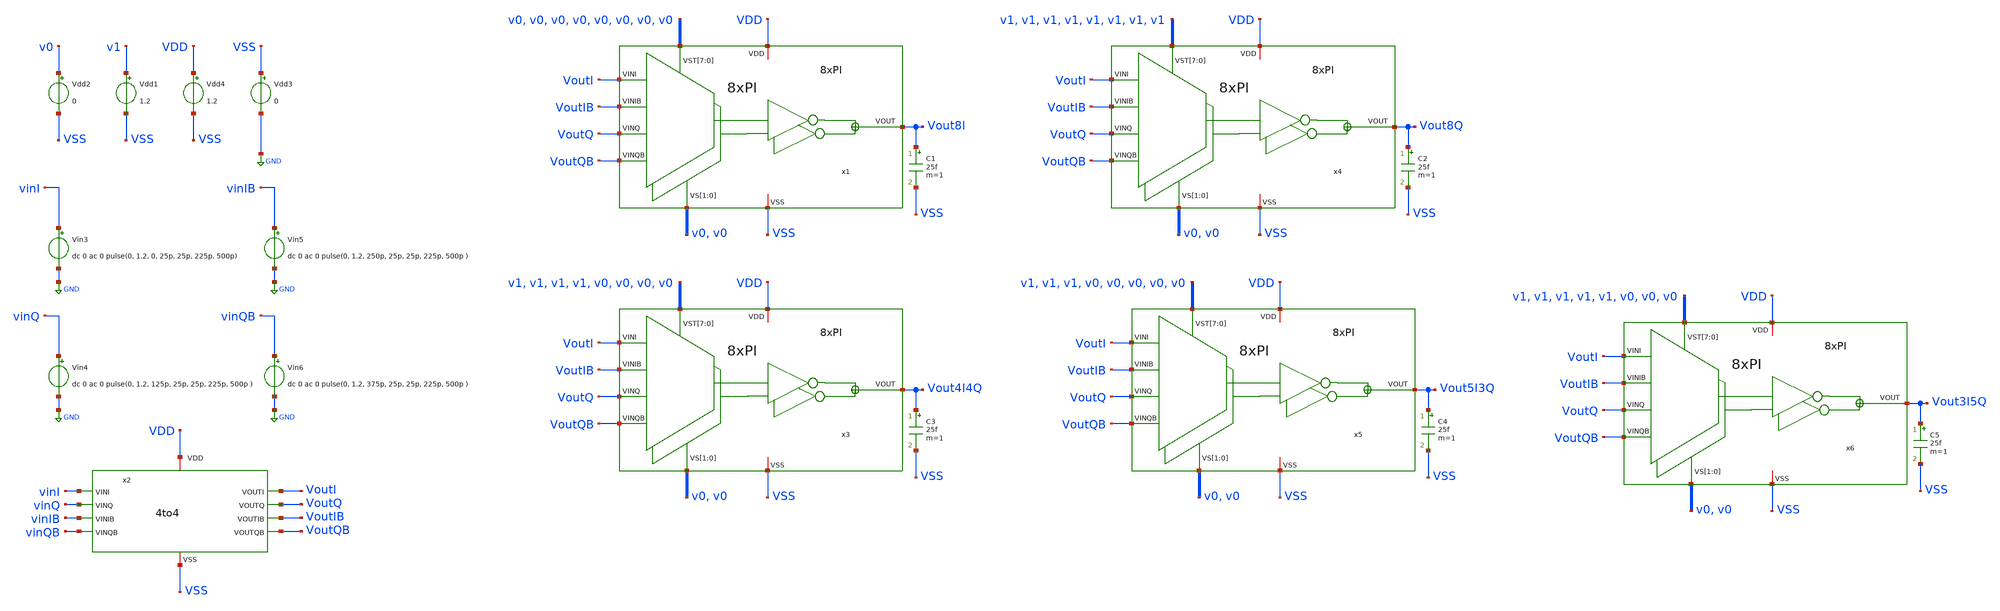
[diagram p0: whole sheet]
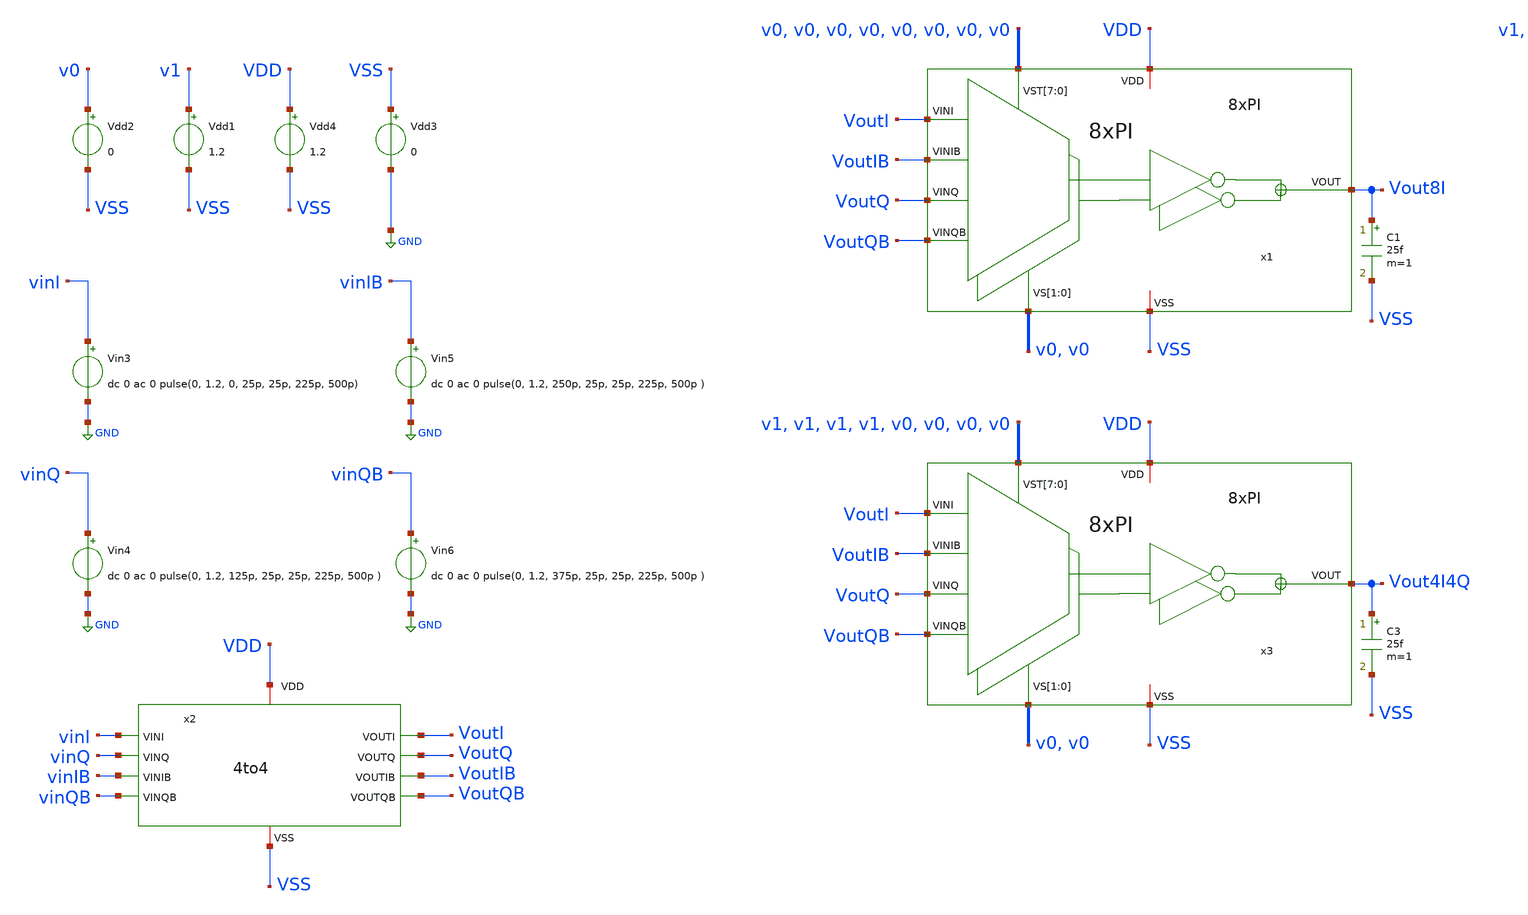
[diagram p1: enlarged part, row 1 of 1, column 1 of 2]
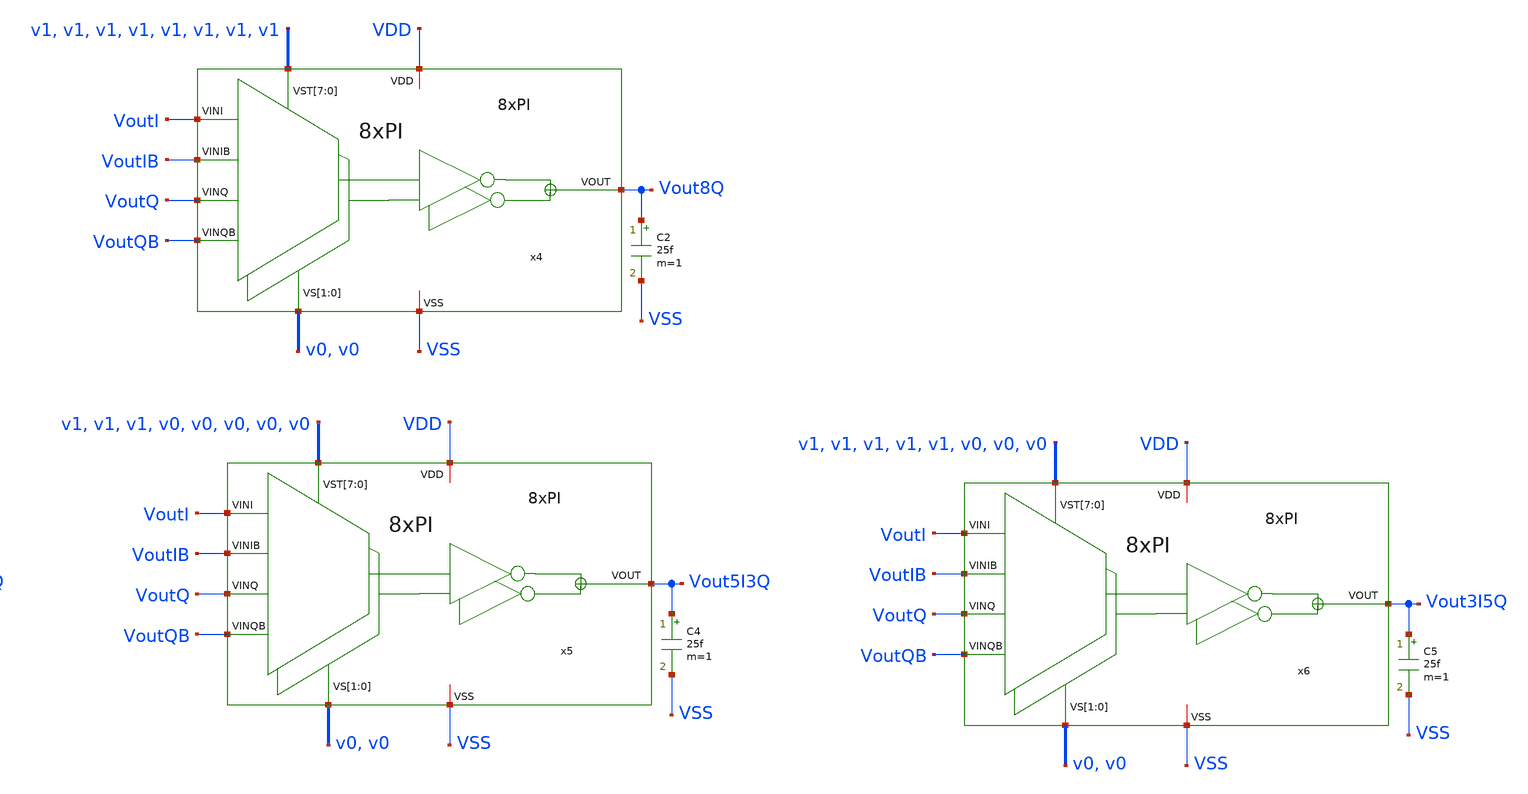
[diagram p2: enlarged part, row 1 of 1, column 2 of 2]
** sch_path: 8xPI/tb_8xPI.sch
**.subckt tb_8xPI
x1 VoutI VoutIB VoutQ VoutQB v0 v0 v0 v0 v0 v0 v0 v0 v0 v0 Vout8I VDD VSS 8xPI
Vin3 vinI GND dc 0 ac 0 pulse(0, 1.2, 0, 25p, 25p, 225p, 500p)
Vin4 vinQ GND dc 0 ac 0 pulse(0, 1.2, 125p, 25p, 25p, 225p, 500p )
Vin5 vinIB GND dc 0 ac 0 pulse(0, 1.2, 250p, 25p, 25p, 225p, 500p )
Vin6 vinQB GND dc 0 ac 0 pulse(0, 1.2, 375p, 25p, 25p, 225p, 500p )
x2 VDD vinI VoutI VoutQ vinQ vinIB VoutIB vinQB VoutQB VSS 4to4
Vdd4 VDD VSS 1.2
Vdd1 v1 VSS 1.2
Vdd2 v0 VSS 0
Vdd3 VSS GND 0
x3 VoutI VoutIB VoutQ VoutQB v0 v0 v1 v1 v1 v1 v0 v0 v0 v0 Vout4I4Q VDD VSS 8xPI
x4 VoutI VoutIB VoutQ VoutQB v0 v0 v1 v1 v1 v1 v1 v1 v1 v1 Vout8Q VDD VSS 8xPI
x5 VoutI VoutIB VoutQ VoutQB v0 v0 v1 v1 v1 v0 v0 v0 v0 v0 Vout5I3Q VDD VSS 8xPI
x6 VoutI VoutIB VoutQ VoutQB v0 v0 v1 v1 v1 v1 v1 v0 v0 v0 Vout3I5Q VDD VSS 8xPI
C1 Vout8I VSS 25f m=1
C2 Vout8Q VSS 25f m=1
C3 Vout4I4Q VSS 25f m=1
C4 Vout5I3Q VSS 25f m=1
C5 Vout3I5Q VSS 25f m=1
**** begin user architecture code


.param temp=27
.control
save all
tran 5p 1.5n

*meas tran tPWI TRIG v(Vout_I) VAl=0.6 RISE=1 TARG v(Vout_I) VAl=0.6 FALL=1
*meas tran tPWIQ TRIG v(Vout_IQ) VAl=0.6 RISE=1 TARG v(Vout_IQ) VAl=0.6 FALL=1
*meas tran tPWQ TRIG v(Vout_Q) VAl=0.6 RISE=1 TARG v(Vout_Q) VAl=0.6 FALL=1
*meas tran tPWQIB TRIG v(Vout_QIB) VAl=0.6 RISE=1 TARG v(Vout_QIB) VAl=0.6 FALL=1
*meas tran tPWIB TRIG v(Vout_IB) VAl=0.6 RISE=1 TARG v(Vout_IB) VAl=0.6 FALL=1
*meas tran tPWIBQB TRIG v(Vout_IBQB) VAl=0.6 RISE=1 TARG v(Vout_IBQB) VAl=0.6 FALL=1
*meas tran tPWQB TRIG v(Vout_QB) VAl=0.6 RISE=1 TARG v(Vout_QB) VAl=0.6 FALL=1
*meas tran tPWQBI TRIG v(Vout_QBI) VAl=0.6 RISE=1 TARG v(Vout_QBI) VAl=0.6 FALL=1


*meas tran tskewI_IQ TRIG v(Vout_I) VAl=0.6 RISE=1 TARG v(Vout_IQ) VAl=0.6 RISE=1
*meas tran tskewIQ_Q TRIG v(Vout_IQ) VAl=0.6 RISE=1 TARG v(Vout_Q) VAl=0.6 RISE=1
*meas tran tskewQ_QIB TRIG v(Vout_Q) VAl=0.6 RISE=1 TARG v(Vout_QIB) VAl=0.6 RISE=1
*meas tran tskewQIB_IB TRIG v(Vout_QIB) VAl=0.6 RISE=1 TARG v(Vout_IB) VAl=0.6 RISE=1
*meas tran tskewIB_IBQB TRIG v(Vout_IB) VAl=0.6 RISE=1 TARG v(Vout_IBQB) VAl=0.6 RISE=1
*meas tran tskewIBQB_QB TRIG v(Vout_IBQB) VAl=0.6 RISE=1 TARG v(Vout_QB) VAl=0.6 RISE=1
*meas tran tskewQB_QBI TRIG v(Vout_QB) VAl=0.6 RISE=1 TARG v(Vout_QBI) VAl=0.6 RISE=1
*meas tran tskewQBI_I TRIG v(Vout_QBI) VAl=0.6 RISE=1 TARG v(Vout_I) VAl=0.6 RISE=2


write tran_8XPI.raw
.endc



.lib cornerMOSlv.lib mos_tt

**** end user architecture code
**.ends

* expanding   symbol:  /foss/designs/PhaseInterpolator/8xPI/8xPI.sym # of pins=9
** sym_path: /foss/designs/PhaseInterpolator/8xPI/8xPI.sym
** sch_path: /foss/designs/PhaseInterpolator/8xPI/8xPI.sch
.subckt 8xPI VINI VINIB VINQ VINQB VS[1] VS[0] VST[7] VST[6] VST[5] VST[4] VST[3] VST[2] VST[1]
+ VST[0] VOUT VDD VSS
*.ipin VINI
*.ipin VINQ
*.ipin VINIB
*.ipin VINQB
*.iopin VDD
*.iopin VSS
*.opin VOUT
*.ipin VS[1],VS[0]
*.ipin VST[7],VST[6],VST[5],VST[4],VST[3],VST[2],VST[1],VST[0]
x1[7] VINI VINIB VDD net1 VS[1] VS[0] VINQ VSS VINQB VST[7] MUX_4_1
x1[6] VINI VINIB VDD net1 VS[1] VS[0] VINQ VSS VINQB VST[6] MUX_4_1
x1[5] VINI VINIB VDD net1 VS[1] VS[0] VINQ VSS VINQB VST[5] MUX_4_1
x1[4] VINI VINIB VDD net1 VS[1] VS[0] VINQ VSS VINQB VST[4] MUX_4_1
x1[3] VINI VINIB VDD net1 VS[1] VS[0] VINQ VSS VINQB VST[3] MUX_4_1
x1[2] VINI VINIB VDD net1 VS[1] VS[0] VINQ VSS VINQB VST[2] MUX_4_1
x1[1] VINI VINIB VDD net1 VS[1] VS[0] VINQ VSS VINQB VST[1] MUX_4_1
x1[0] VINI VINIB VDD net1 VS[1] VS[0] VINQ VSS VINQB VST[0] MUX_4_1
x2 VDD net2 net1 VSS inv
x3[1] VDD net3[1] net2 VSS inv
x3[0] VDD net3[0] net2 VSS inv
x4[3] VDD net4[3] net3[1] VSS inv
x4[2] VDD net4[2] net3[0] VSS inv
x4[1] VDD net4[1] net3[1] VSS inv
x4[0] VDD net4[0] net3[0] VSS inv
x5[7] VDD VOUT net4[3] VSS inv
x5[6] VDD VOUT net4[2] VSS inv
x5[5] VDD VOUT net4[1] VSS inv
x5[4] VDD VOUT net4[0] VSS inv
x5[3] VDD VOUT net4[3] VSS inv
x5[2] VDD VOUT net4[2] VSS inv
x5[1] VDD VOUT net4[1] VSS inv
x5[0] VDD VOUT net4[0] VSS inv
.ends


* expanding   symbol:  4to4.sym # of pins=10
** sym_path: 4to4.sym
** sch_path: 4to4.sch
.subckt 4to4 VDD VINI VOUTI VOUTQ VINQ VINIB VOUTIB VINQB VOUTQB VSS
*.iopin VDD
*.iopin VSS
*.ipin VINI
*.ipin VINQ
*.ipin VINIB
*.ipin VINQB
*.opin VOUTI
*.opin VOUTQ
*.opin VOUTIB
*.opin VOUTQB
x0[7] VDD net4[7] VINI VSS inv
x0[6] VDD net4[6] VINI VSS inv
x0[5] VDD net4[5] VINI VSS inv
x0[4] VDD net4[4] VINI VSS inv
x0[3] VDD net4[3] VINI VSS inv
x0[2] VDD net4[2] VINI VSS inv
x0[1] VDD net4[1] VINI VSS inv
x0[0] VDD net4[0] VINI VSS inv
x1[7] VDD net3[7] VINQ VSS inv
x1[6] VDD net3[6] VINQ VSS inv
x1[5] VDD net3[5] VINQ VSS inv
x1[4] VDD net3[4] VINQ VSS inv
x1[3] VDD net3[3] VINQ VSS inv
x1[2] VDD net3[2] VINQ VSS inv
x1[1] VDD net3[1] VINQ VSS inv
x1[0] VDD net3[0] VINQ VSS inv
x2[7] VDD net1[7] VINIB VSS inv
x2[6] VDD net1[6] VINIB VSS inv
x2[5] VDD net1[5] VINIB VSS inv
x2[4] VDD net1[4] VINIB VSS inv
x2[3] VDD net1[3] VINIB VSS inv
x2[2] VDD net1[2] VINIB VSS inv
x2[1] VDD net1[1] VINIB VSS inv
x2[0] VDD net1[0] VINIB VSS inv
x3[7] VDD net2[7] VINQB VSS inv
x3[6] VDD net2[6] VINQB VSS inv
x3[5] VDD net2[5] VINQB VSS inv
x3[4] VDD net2[4] VINQB VSS inv
x3[3] VDD net2[3] VINQB VSS inv
x3[2] VDD net2[2] VINQB VSS inv
x3[1] VDD net2[1] VINQB VSS inv
x3[0] VDD net2[0] VINQB VSS inv
x4[15] VDD VOUTI net4[7] VSS inv
x4[14] VDD VOUTI net4[6] VSS inv
x4[13] VDD VOUTI net4[5] VSS inv
x4[12] VDD VOUTI net4[4] VSS inv
x4[11] VDD VOUTI net4[3] VSS inv
x4[10] VDD VOUTI net4[2] VSS inv
x4[9] VDD VOUTI net4[1] VSS inv
x4[8] VDD VOUTI net4[0] VSS inv
x4[7] VDD VOUTI net4[7] VSS inv
x4[6] VDD VOUTI net4[6] VSS inv
x4[5] VDD VOUTI net4[5] VSS inv
x4[4] VDD VOUTI net4[4] VSS inv
x4[3] VDD VOUTI net4[3] VSS inv
x4[2] VDD VOUTI net4[2] VSS inv
x4[1] VDD VOUTI net4[1] VSS inv
x4[0] VDD VOUTI net4[0] VSS inv
x5[15] VDD VOUTQ net3[7] VSS inv
x5[14] VDD VOUTQ net3[6] VSS inv
x5[13] VDD VOUTQ net3[5] VSS inv
x5[12] VDD VOUTQ net3[4] VSS inv
x5[11] VDD VOUTQ net3[3] VSS inv
x5[10] VDD VOUTQ net3[2] VSS inv
x5[9] VDD VOUTQ net3[1] VSS inv
x5[8] VDD VOUTQ net3[0] VSS inv
x5[7] VDD VOUTQ net3[7] VSS inv
x5[6] VDD VOUTQ net3[6] VSS inv
x5[5] VDD VOUTQ net3[5] VSS inv
x5[4] VDD VOUTQ net3[4] VSS inv
x5[3] VDD VOUTQ net3[3] VSS inv
x5[2] VDD VOUTQ net3[2] VSS inv
x5[1] VDD VOUTQ net3[1] VSS inv
x5[0] VDD VOUTQ net3[0] VSS inv
x6[15] VDD VOUTIB net1[7] VSS inv
x6[14] VDD VOUTIB net1[6] VSS inv
x6[13] VDD VOUTIB net1[5] VSS inv
x6[12] VDD VOUTIB net1[4] VSS inv
x6[11] VDD VOUTIB net1[3] VSS inv
x6[10] VDD VOUTIB net1[2] VSS inv
x6[9] VDD VOUTIB net1[1] VSS inv
x6[8] VDD VOUTIB net1[0] VSS inv
x6[7] VDD VOUTIB net1[7] VSS inv
x6[6] VDD VOUTIB net1[6] VSS inv
x6[5] VDD VOUTIB net1[5] VSS inv
x6[4] VDD VOUTIB net1[4] VSS inv
x6[3] VDD VOUTIB net1[3] VSS inv
x6[2] VDD VOUTIB net1[2] VSS inv
x6[1] VDD VOUTIB net1[1] VSS inv
x6[0] VDD VOUTIB net1[0] VSS inv
x7[15] VDD VOUTQB net2[7] VSS inv
x7[14] VDD VOUTQB net2[6] VSS inv
x7[13] VDD VOUTQB net2[5] VSS inv
x7[12] VDD VOUTQB net2[4] VSS inv
x7[11] VDD VOUTQB net2[3] VSS inv
x7[10] VDD VOUTQB net2[2] VSS inv
x7[9] VDD VOUTQB net2[1] VSS inv
x7[8] VDD VOUTQB net2[0] VSS inv
x7[7] VDD VOUTQB net2[7] VSS inv
x7[6] VDD VOUTQB net2[6] VSS inv
x7[5] VDD VOUTQB net2[5] VSS inv
x7[4] VDD VOUTQB net2[4] VSS inv
x7[3] VDD VOUTQB net2[3] VSS inv
x7[2] VDD VOUTQB net2[2] VSS inv
x7[1] VDD VOUTQB net2[1] VSS inv
x7[0] VDD VOUTQB net2[0] VSS inv
.ends


* expanding   symbol:  /foss/designs/PhaseInterpolator/Custom_std_cells/MUX_4_1.sym # of pins=9
** sym_path: /foss/designs/PhaseInterpolator/Custom_std_cells/MUX_4_1.sym
** sch_path: /foss/designs/PhaseInterpolator/Custom_std_cells/MUX_4_1.sch
.subckt MUX_4_1 VINA VINB VDD VOUT VS[1] VS[0] VINC VSS VIND VST
*.opin VOUT
*.iopin VDD
*.iopin VSS
*.ipin VINA
*.ipin VINB
*.ipin VINC
*.ipin VIND
*.ipin VS[1],VS[0]
*.ipin VST
x3 VDD VINC net2 VS[1] VIND VSS MUX_2_1
x4 VDD VINA net1 VS[0] VINB VSS MUX_2_1
x5 VDD net1 VOUT VST net2 VSS MUX_2_1
.ends


* expanding   symbol:  /foss/designs/PhaseInterpolator/Custom_std_cells/MUX_2_1.sym # of pins=6
** sym_path: /foss/designs/PhaseInterpolator/Custom_std_cells/MUX_2_1.sym
** sch_path: /foss/designs/PhaseInterpolator/Custom_std_cells/MUX_2_1.sch
.subckt MUX_2_1 VDD VINA VOUT VS VINB VSS
*.opin VOUT
*.ipin VINA
*.ipin VINB
*.ipin VS
*.iopin VDD
*.iopin VSS
x1 VOUT net1 VS VINA VDD VSS tg_custom
x2 VOUT VS net1 VINB VDD VSS tg_custom
x3 VDD net1 VS VSS inv
.ends


* expanding   symbol:  /foss/designs/PhaseInterpolator/Custom_std_cells/tg_custom.sym # of pins=6
** sym_path: /foss/designs/PhaseInterpolator/Custom_std_cells/tg_custom.sym
** sch_path: /foss/designs/PhaseInterpolator/Custom_std_cells/tg_custom.sch
.subckt tg_custom VOUT VSN VSP VIN VBP VBN
*.iopin VIN
*.iopin VSN
*.iopin VOUT
*.iopin VSP
*.iopin VBN
*.iopin VBP
XM1 VOUT VSN VIN VBN sg13_lv_nmos w=0.15u l=0.13u ng=1 m=1 mm_ok=1
XM2 VOUT VSP VIN VBP sg13_lv_pmos w=0.15u l=0.13u ng=1 m=2 mm_ok=1
.ends

.GLOBAL GND
.end
